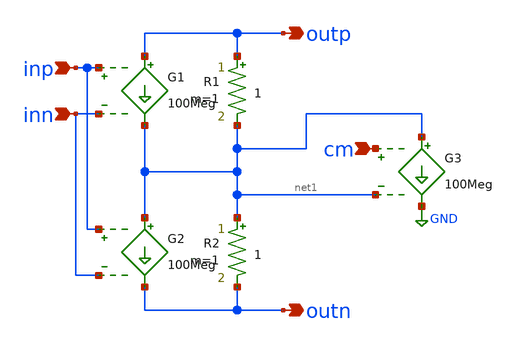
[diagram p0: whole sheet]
** sch_path: prj/template/2_Idealized_circuits/ideal_differential_opamp.sch
**.subckt ideal_differential_opamp outp inp inn outn cm
*.opin outp
*.ipin inp
*.ipin inn
*.opin outn
*.ipin cm
G1 outp net1 inp inn 100Meg
R1 outp net1 1 m=1
G2 net1 outn inp inn 100Meg
R2 net1 outn 1 m=1
G3 net1 GND cm net1 100Meg
**.ends
.GLOBAL GND
.end
